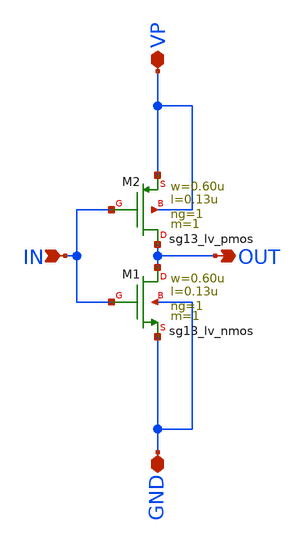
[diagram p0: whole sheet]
** sch_path: PLL0663-main/schematic/xschem/divider/inverter_x4_top.sch
**.subckt inverter_x4_top IN VP OUT GND
*.ipin IN
*.iopin VP
*.opin OUT
*.iopin GND
XM1 OUT IN GND GND sg13_lv_nmos w=0.60u l=0.13u ng=1 m=1 mm_ok=1
XM2 OUT IN VP VP sg13_lv_pmos w=0.60u l=0.13u ng=1 m=1 mm_ok=1
**.ends
.end
